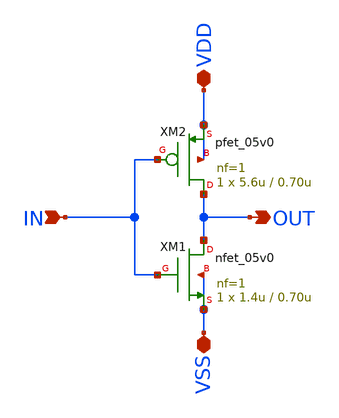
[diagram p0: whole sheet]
** sch_path: design/schematics/ADC/Non_Overlapping_clk_gen/SG_B11_cic_bms_afe_inv_1x.sch
**.subckt SG_B11_cic_bms_afe_inv_1x OUT VSS VDD IN
*.opin OUT
*.iopin VSS
*.iopin VDD
*.ipin IN
XM1 OUT IN VSS VSS nfet_05v0 L=0.70u W=1.4u nf=1 ad='int((nf+1)/2) * W/nf * 0.18u' as='int((nf+2)/2) * W/nf * 0.18u'
+ pd='2*int((nf+1)/2) * (W/nf + 0.18u)' ps='2*int((nf+2)/2) * (W/nf + 0.18u)' nrd='0.18u / W' nrs='0.18u / W'
+ sa=0 sb=0 sd=0 m=1
XM2 OUT IN VDD VDD pfet_05v0 L=0.70u W=5.6u nf=1 ad='int((nf+1)/2) * W/nf * 0.18u' as='int((nf+2)/2) * W/nf * 0.18u'
+ pd='2*int((nf+1)/2) * (W/nf + 0.18u)' ps='2*int((nf+2)/2) * (W/nf + 0.18u)' nrd='0.18u / W' nrs='0.18u / W'
+ sa=0 sb=0 sd=0 m=1
**.ends
.end
